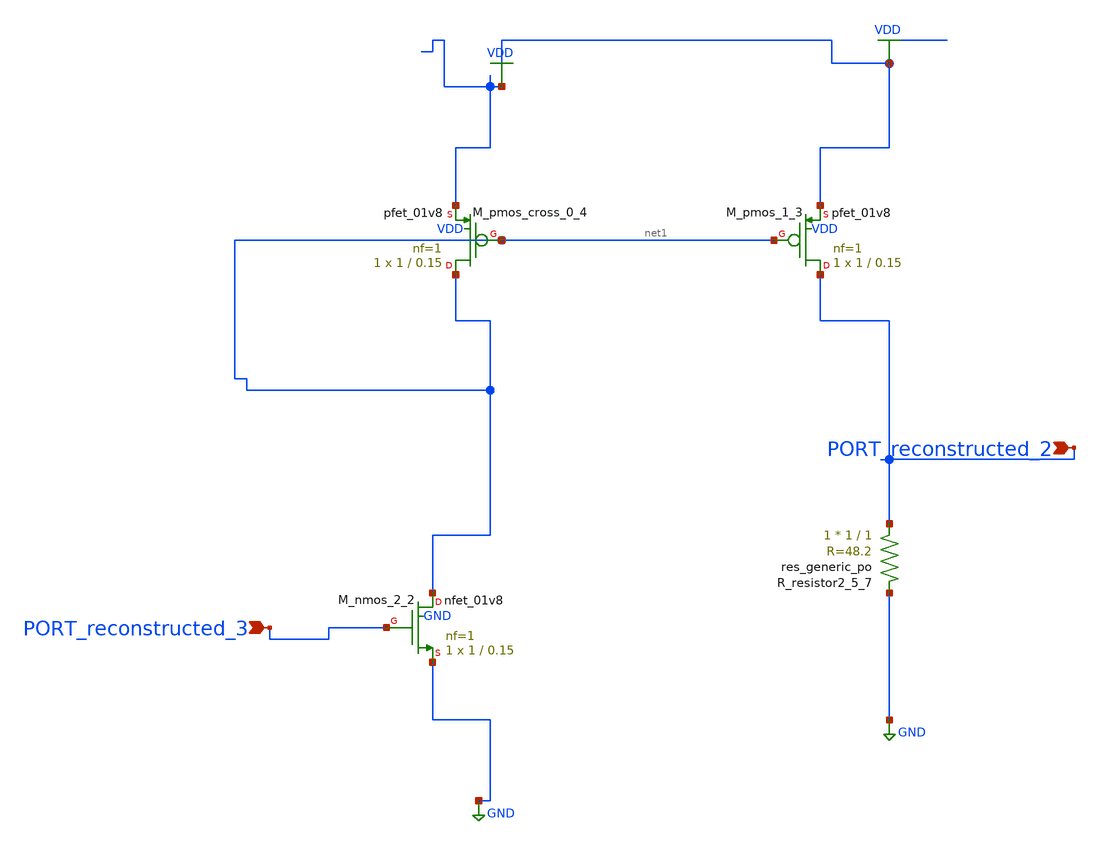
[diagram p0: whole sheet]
** sch_path: schematics/AMSNet/256.sch
**.subckt 256 PORT_reconstructed_2 PORT_reconstructed_3
*.ipin PORT_reconstructed_2
*.ipin PORT_reconstructed_3
XM_nmos_2_2 net1 PORT_reconstructed_3 GND GND sky130_fd_pr__nfet_01v8 L=0.15 W=1 nf=1 ad='int((1 + 1)/2) * 1 / 1 * 0.29'
+ as='int((1 + 2)/2) * 1 / 1 * 0.29' pd='2*int((1 + 1)/2) * (1 / 1 + 0.29)' ps='2*int((1 + 2)/2) * (1 / 1 + 0.29)'
+ nrd='0.29 / 1 ' nrs='0.29 / 1 ' sa=0 sb=0 sd=0 mult=1 m=1
XM_pmos_1_3 PORT_reconstructed_2 net1 VDD VDD sky130_fd_pr__pfet_01v8 L=0.15 W=1 nf=1 ad='int((1 + 1)/2) * 1 / 1 * 0.29'
+ as='int((1 + 2)/2) * 1 / 1 * 0.29' pd='2*int((1 + 1)/2) * (1 / 1 + 0.29)' ps='2*int((1 + 2)/2) * (1 / 1 + 0.29)'
+ nrd='0.29 / 1 ' nrs='0.29 / 1 ' sa=0 sb=0 sd=0 mult=1 m=1
XM_pmos_cross_0_4 net1 net1 VDD VDD sky130_fd_pr__pfet_01v8 L=0.15 W=1 nf=1 ad='int((1 + 1)/2) * 1 / 1 * 0.29'
+ as='int((1 + 2)/2) * 1 / 1 * 0.29' pd='2*int((1 + 1)/2) * (1 / 1 + 0.29)' ps='2*int((1 + 2)/2) * (1 / 1 + 0.29)'
+ nrd='0.29 / 1 ' nrs='0.29 / 1 ' sa=0 sb=0 sd=0 mult=1 m=1
XR_resistor2_5_7 PORT_reconstructed_2 GND sky130_fd_pr__res_generic_po W=1 L=1 m=1
**.ends
.GLOBAL GND
.GLOBAL VDD
.end
